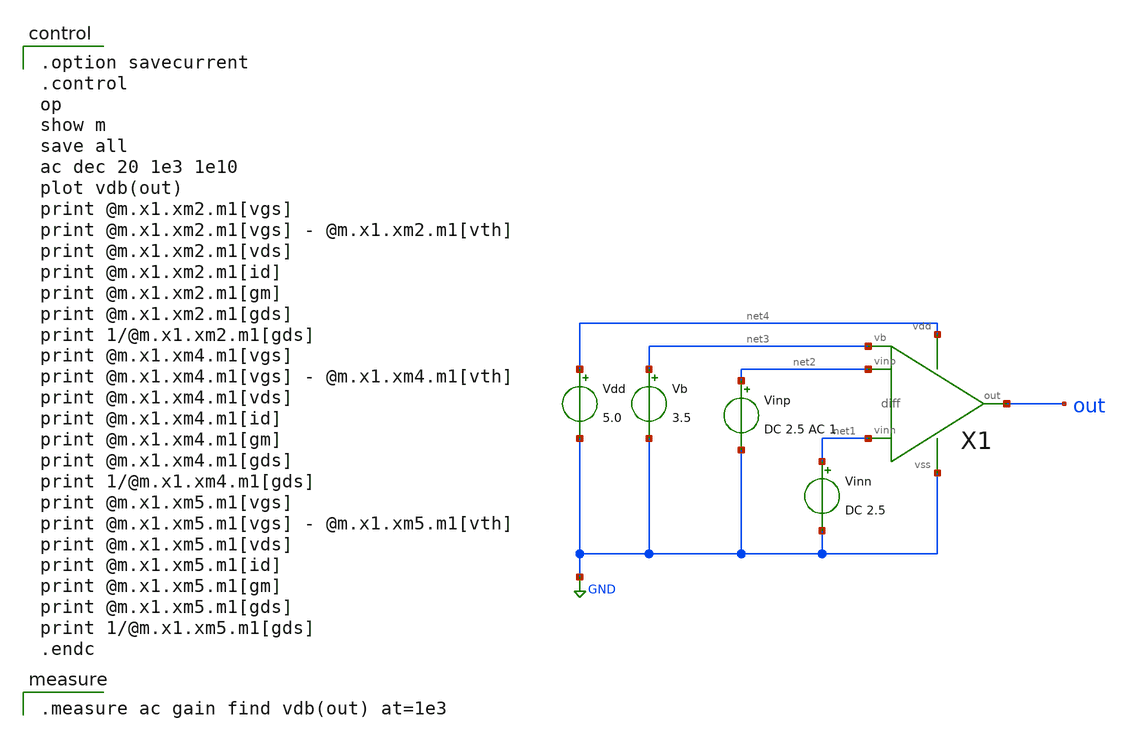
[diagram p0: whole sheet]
** sch_path: schematic/20250924_OSS_Workshop/ishikai/opamp/sample/diff_ac.sch
**.subckt diff_ac
Vdd net4 GND 5.0
Vb net3 GND 3.5
Vinn net1 GND DC 2.5
Vinp net2 GND DC 2.5 AC 1
X1 net2 net1 out net4 GND net3 diff
**** begin user architecture code

.option savecurrent
.control
op
show m
save all
ac dec 20 1e3 1e10
plot vdb(out)
print @m.x1.xm2.m1[vgs]
print @m.x1.xm2.m1[vgs] - @m.x1.xm2.m1[vth]
print @m.x1.xm2.m1[vds]
print @m.x1.xm2.m1[id]
print @m.x1.xm2.m1[gm]
print @m.x1.xm2.m1[gds]
print 1/@m.x1.xm2.m1[gds]
print @m.x1.xm4.m1[vgs]
print @m.x1.xm4.m1[vgs] - @m.x1.xm4.m1[vth]
print @m.x1.xm4.m1[vds]
print @m.x1.xm4.m1[id]
print @m.x1.xm4.m1[gm]
print @m.x1.xm4.m1[gds]
print 1/@m.x1.xm4.m1[gds]
print @m.x1.xm5.m1[vgs]
print @m.x1.xm5.m1[vgs] - @m.x1.xm5.m1[vth]
print @m.x1.xm5.m1[vds]
print @m.x1.xm5.m1[id]
print @m.x1.xm5.m1[gm]
print @m.x1.xm5.m1[gds]
print 1/@m.x1.xm5.m1[gds]
.endc


.measure ac gain find vdb(out) at=1e3

 .include $::LIB/../ip62_models
**** end user architecture code
**.ends

* expanding   symbol:  diff.sym # of pins=6
** sym_path: schematic/20250924_OSS_Workshop/ishikai/opamp/sample/diff.sym
** sch_path: schematic/20250924_OSS_Workshop/ishikai/opamp/sample/diff.sch
.subckt diff vinp vinn out vdd vss vb
*.ipin vinn
*.ipin vinp
*.ipin vb
*.opin out
*.iopin vdd
*.iopin vss
XM5 net2 vb vdd vdd PMOS w=180u l=1u as=0 ad=0 ps=0 pd=0 nrd=0 nrs=0 m=1
XM1 net1 vinn net2 net2 PMOS w=360u l=1u as=0 ad=0 ps=0 pd=0 nrd=0 nrs=0 m=1
XM2 out vinp net2 net2 PMOS w=360u l=1u as=0 ad=0 ps=0 pd=0 nrd=0 nrs=0 m=1
XM3 net1 net1 vss vss NMOS w=30u l=1u as=0 ad=0 ps=0 pd=0 nrd=0 nrs=0 m=1
XM4 out net1 vss vss NMOS w=30u l=1u as=0 ad=0 ps=0 pd=0 nrd=0 nrs=0 m=1
.ends

.GLOBAL GND
.end
